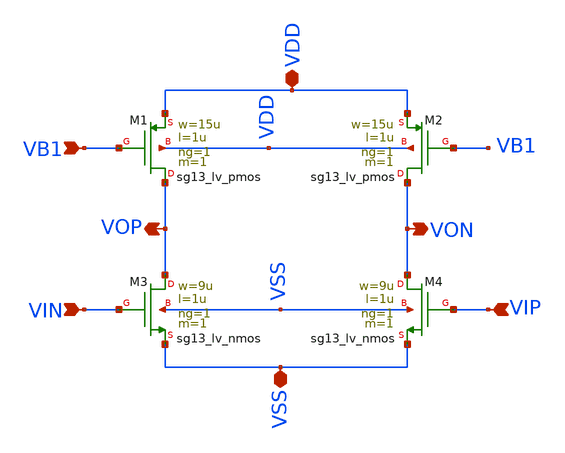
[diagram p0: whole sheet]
** sch_path: BTDay8-Ex/AMP_CS_08V.sch
**.subckt AMP_CS_08V VDD VIN VIP VSS VB1 VOP VON
*.iopin VDD
*.ipin VIN
*.ipin VIP
*.iopin VSS
*.ipin VB1
*.opin VOP
*.opin VON
XM1 VOP VB1 VDD VDD sg13_lv_pmos w=15u l=1u ng=1 m=1 mm_ok=1
XM2 VON VB1 VDD VDD sg13_lv_pmos w=15u l=1u ng=1 m=1 mm_ok=1
XM3 VOP VIN VSS VSS sg13_lv_nmos w=9u l=1u ng=1 m=1 mm_ok=1
XM4 VON VIP VSS VSS sg13_lv_nmos w=9u l=1u ng=1 m=1 mm_ok=1
**.ends
.end
